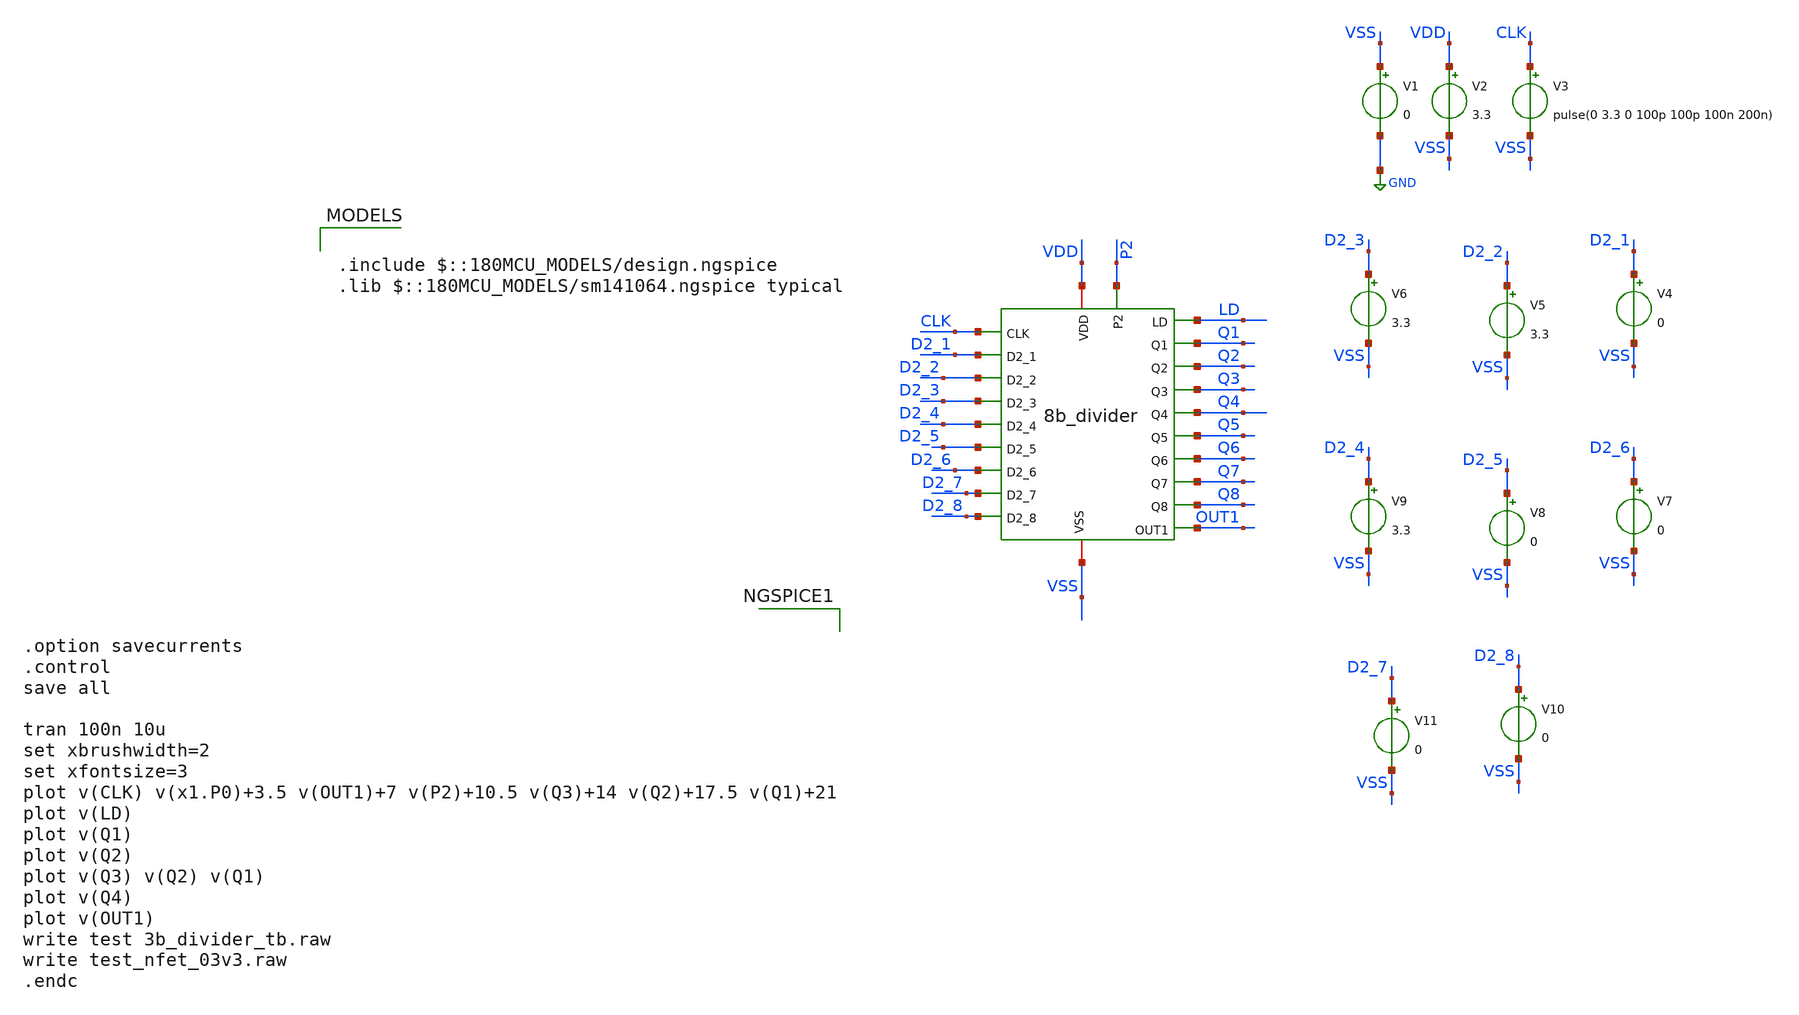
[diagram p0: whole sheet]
** sch_path: Clock_Generator_PAKISTAN_06/Schematics/8b_divider_tb.sch
**.subckt 8b_divider_tb
x1 VDD LD CLK D2_1 Q1 D2_2 Q2 D2_3 Q3 D2_4 Q4 D2_5 Q5 D2_6 Q6 D2_7 Q7 D2_8 Q8 VSS OUT1 P2 8b_divider
V1 VSS GND 0
V2 VDD VSS 3.3
V3 CLK VSS pulse(0 3.3 0 100p 100p 100n 200n)
V4 D2_1 VSS 0
V5 D2_2 VSS 3.3
V6 D2_3 VSS 3.3
V7 D2_6 VSS 0
V8 D2_5 VSS 0
V9 D2_4 VSS 3.3
V10 D2_8 VSS 0
V11 D2_7 VSS 0
**** begin user architecture code

.include $::180MCU_MODELS/design.ngspice
.lib $::180MCU_MODELS/sm141064.ngspice typical



.option savecurrents
.control
save all

tran 100n 10u
set xbrushwidth=2
set xfontsize=3
plot v(CLK) v(x1.P0)+3.5 v(OUT1)+7 v(P2)+10.5 v(Q3)+14 v(Q2)+17.5 v(Q1)+21
plot v(LD)
plot v(Q1)
plot v(Q2)
plot v(Q3) v(Q2) v(Q1)
plot v(Q4)
plot v(OUT1)
write test 3b_divider_tb.raw
write test_nfet_03v3.raw
.endc


**** end user architecture code
**.ends
.GLOBAL GND
.end
